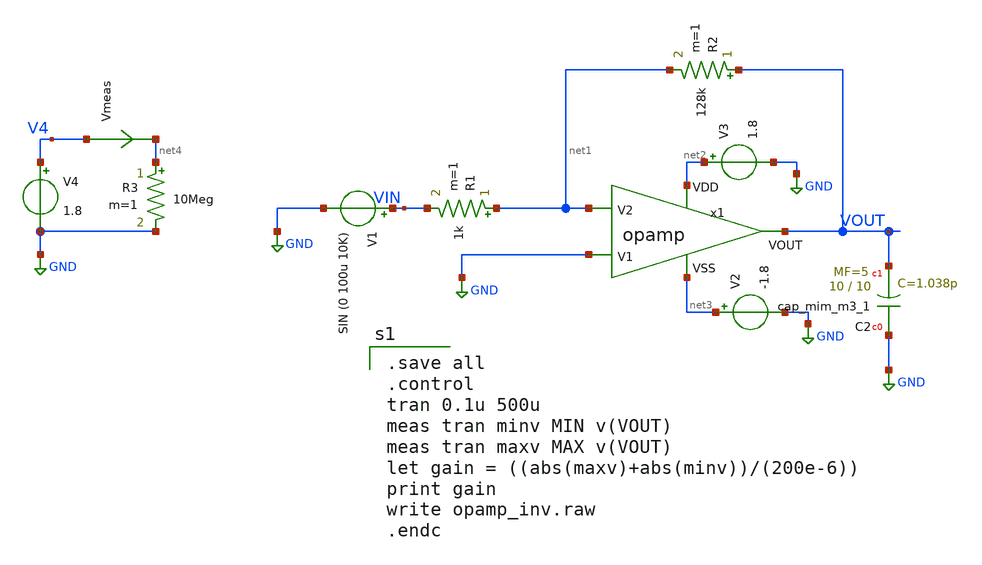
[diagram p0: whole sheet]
** sch_path: opamp_inv.sch
**.subckt opamp_inv
V1 VIN GND SIN (0 100u 10K)
V2 net3 GND -1.8
V3 net2 GND 1.8
x1 net2 net3 GND net1 VOUT opamp
R1 net1 VIN 1k m=1
R2 VOUT net1 128k m=1
V4 V4 GND 1.8
R3 net4 GND 10Meg m=1
Vmeas V4 net4 0
.save i(vmeas)
XC2 GND VOUT sky130_fd_pr__cap_mim_m3_1 W=10 L=10 MF=5 m=5
**** begin user architecture code

.save all
.control
tran 0.1u 500u
meas tran minv MIN v(VOUT)
meas tran maxv MAX v(VOUT)
let gain = ((abs(maxv)+abs(minv))/(200e-6))
print gain
write opamp_inv.raw
.endc


** opencircuitdesign pdks install
.lib $::SKYWATER_MODELS/sky130.lib.spice tt


**** end user architecture code
**.ends

* expanding   symbol:  ../xschem/opamp.sym # of pins=5
** sym_path: ../xschem/opamp.sym
** sch_path: ../xschem/opamp.sch
.subckt opamp VDD VSS V1 V2 VOUT
*.ipin VSS
*.ipin VDD
*.ipin V2
*.ipin V1
*.opin VOUT
XM2 net2 V2 net1 VSS sky130_fd_pr__nfet_g5v0d10v5 L=1 W=17.45 nf=1 ad='int((nf+1)/2) * W/nf * 0.29' as='int((nf+2)/2) * W/nf * 0.29'
+ pd='2*int((nf+1)/2) * (W/nf + 0.29)' ps='2*int((nf+2)/2) * (W/nf + 0.29)' nrd='0.29 / W' nrs='0.29 / W'
+ sa=0 sb=0 sd=0 mult=1 m=1
XM1 net3 net2 VDD VDD sky130_fd_pr__pfet_g5v0d10v5 L=1 W=30 nf=1 ad='int((nf+1)/2) * W/nf * 0.29' as='int((nf+2)/2) * W/nf * 0.29'
+ pd='2*int((nf+1)/2) * (W/nf + 0.29)' ps='2*int((nf+2)/2) * (W/nf + 0.29)' nrd='0.29 / W' nrs='0.29 / W'
+ sa=0 sb=0 sd=0 mult=1 m=1
XM4 net3 V1 net1 VSS sky130_fd_pr__nfet_g5v0d10v5 L=1 W=17.45 nf=1 ad='int((nf+1)/2) * W/nf * 0.29' as='int((nf+2)/2) * W/nf * 0.29'
+ pd='2*int((nf+1)/2) * (W/nf + 0.29)' ps='2*int((nf+2)/2) * (W/nf + 0.29)' nrd='0.29 / W' nrs='0.29 / W'
+ sa=0 sb=0 sd=0 mult=1 m=1
XM5 net6 net4 VSS VSS sky130_fd_pr__nfet_g5v0d10v5 L=1 W=15.17 nf=1 ad='int((nf+1)/2) * W/nf * 0.29'
+ as='int((nf+2)/2) * W/nf * 0.29' pd='2*int((nf+1)/2) * (W/nf + 0.29)' ps='2*int((nf+2)/2) * (W/nf + 0.29)'
+ nrd='0.29 / W' nrs='0.29 / W' sa=0 sb=0 sd=0 mult=1 m=1
XM6 net8 net4 VSS VSS sky130_fd_pr__nfet_g5v0d10v5 L=1 W=19 nf=1 ad='int((nf+1)/2) * W/nf * 0.29' as='int((nf+2)/2) * W/nf * 0.29'
+ pd='2*int((nf+1)/2) * (W/nf + 0.29)' ps='2*int((nf+2)/2) * (W/nf + 0.29)' nrd='0.29 / W' nrs='0.29 / W'
+ sa=0 sb=0 sd=0 mult=1 m=1
XM7 net4 net4 VSS VSS sky130_fd_pr__nfet_g5v0d10v5 L=1 W=15.17 nf=1 ad='int((nf+1)/2) * W/nf * 0.29'
+ as='int((nf+2)/2) * W/nf * 0.29' pd='2*int((nf+1)/2) * (W/nf + 0.29)' ps='2*int((nf+2)/2) * (W/nf + 0.29)'
+ nrd='0.29 / W' nrs='0.29 / W' sa=0 sb=0 sd=0 mult=1 m=1
XM3 net2 net2 VDD VDD sky130_fd_pr__pfet_g5v0d10v5 L=1 W=30 nf=1 ad='int((nf+1)/2) * W/nf * 0.29' as='int((nf+2)/2) * W/nf * 0.29'
+ pd='2*int((nf+1)/2) * (W/nf + 0.29)' ps='2*int((nf+2)/2) * (W/nf + 0.29)' nrd='0.29 / W' nrs='0.29 / W'
+ sa=0 sb=0 sd=0 mult=1 m=1
XM8 VOUT net3 VDD VDD sky130_fd_pr__pfet_g5v0d10v5 L=1 W=38 nf=1 ad='int((nf+1)/2) * W/nf * 0.29' as='int((nf+2)/2) * W/nf * 0.29'
+ pd='2*int((nf+1)/2) * (W/nf + 0.29)' ps='2*int((nf+2)/2) * (W/nf + 0.29)' nrd='0.29 / W' nrs='0.29 / W'
+ sa=0 sb=0 sd=0 mult=2 m=2
XC1 net5 net3 sky130_fd_pr__cap_mim_m3_1 W=9 L=9 MF=2 m=2
V_ibias net7 net4 0
.save i(v_ibias)
XR3 net5 VOUT VSS sky130_fd_pr__res_high_po_0p69 L=3.2 mult=1 m=1
V_ibias1 net1 net6 0
.save i(v_ibias1)
I1 net9 net10 63.26u
V_iout VOUT net8 0
.save i(v_iout)
XM9 VDD VDD net7 VSS sky130_fd_pr__nfet_g5v0d10v5 L=1 W=0.69 nf=1 ad='int((nf+1)/2) * W/nf * 0.29' as='int((nf+2)/2) * W/nf * 0.29'
+ pd='2*int((nf+1)/2) * (W/nf + 0.29)' ps='2*int((nf+2)/2) * (W/nf + 0.29)' nrd='0.29 / W' nrs='0.29 / W'
+ sa=0 sb=0 sd=0 mult=1 m=1
.ends

.GLOBAL GND
.end
